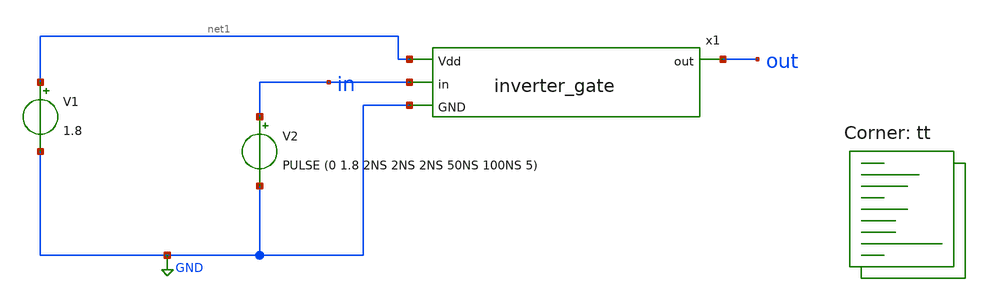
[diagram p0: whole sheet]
** sch_path: INVERTER/xschem/inverter_tb_hirarki.sch
**.subckt inverter_tb_hirarki
V1 net1 GND 1.8
V2 in GND PULSE (0 1.8 2NS 2NS 2NS 50NS 100NS 5)
x1 net1 in out GND inverter_gate
**** begin user architecture code
.lib $::SKYWATER_MODELS/sky130.lib.spice tt


.option wnflag=0
.option savecurrents
.control
save all
tran 1ns 200ns
plot in out
op
.endc


**** end user architecture code
**.ends
.GLOBAL GND
.end
